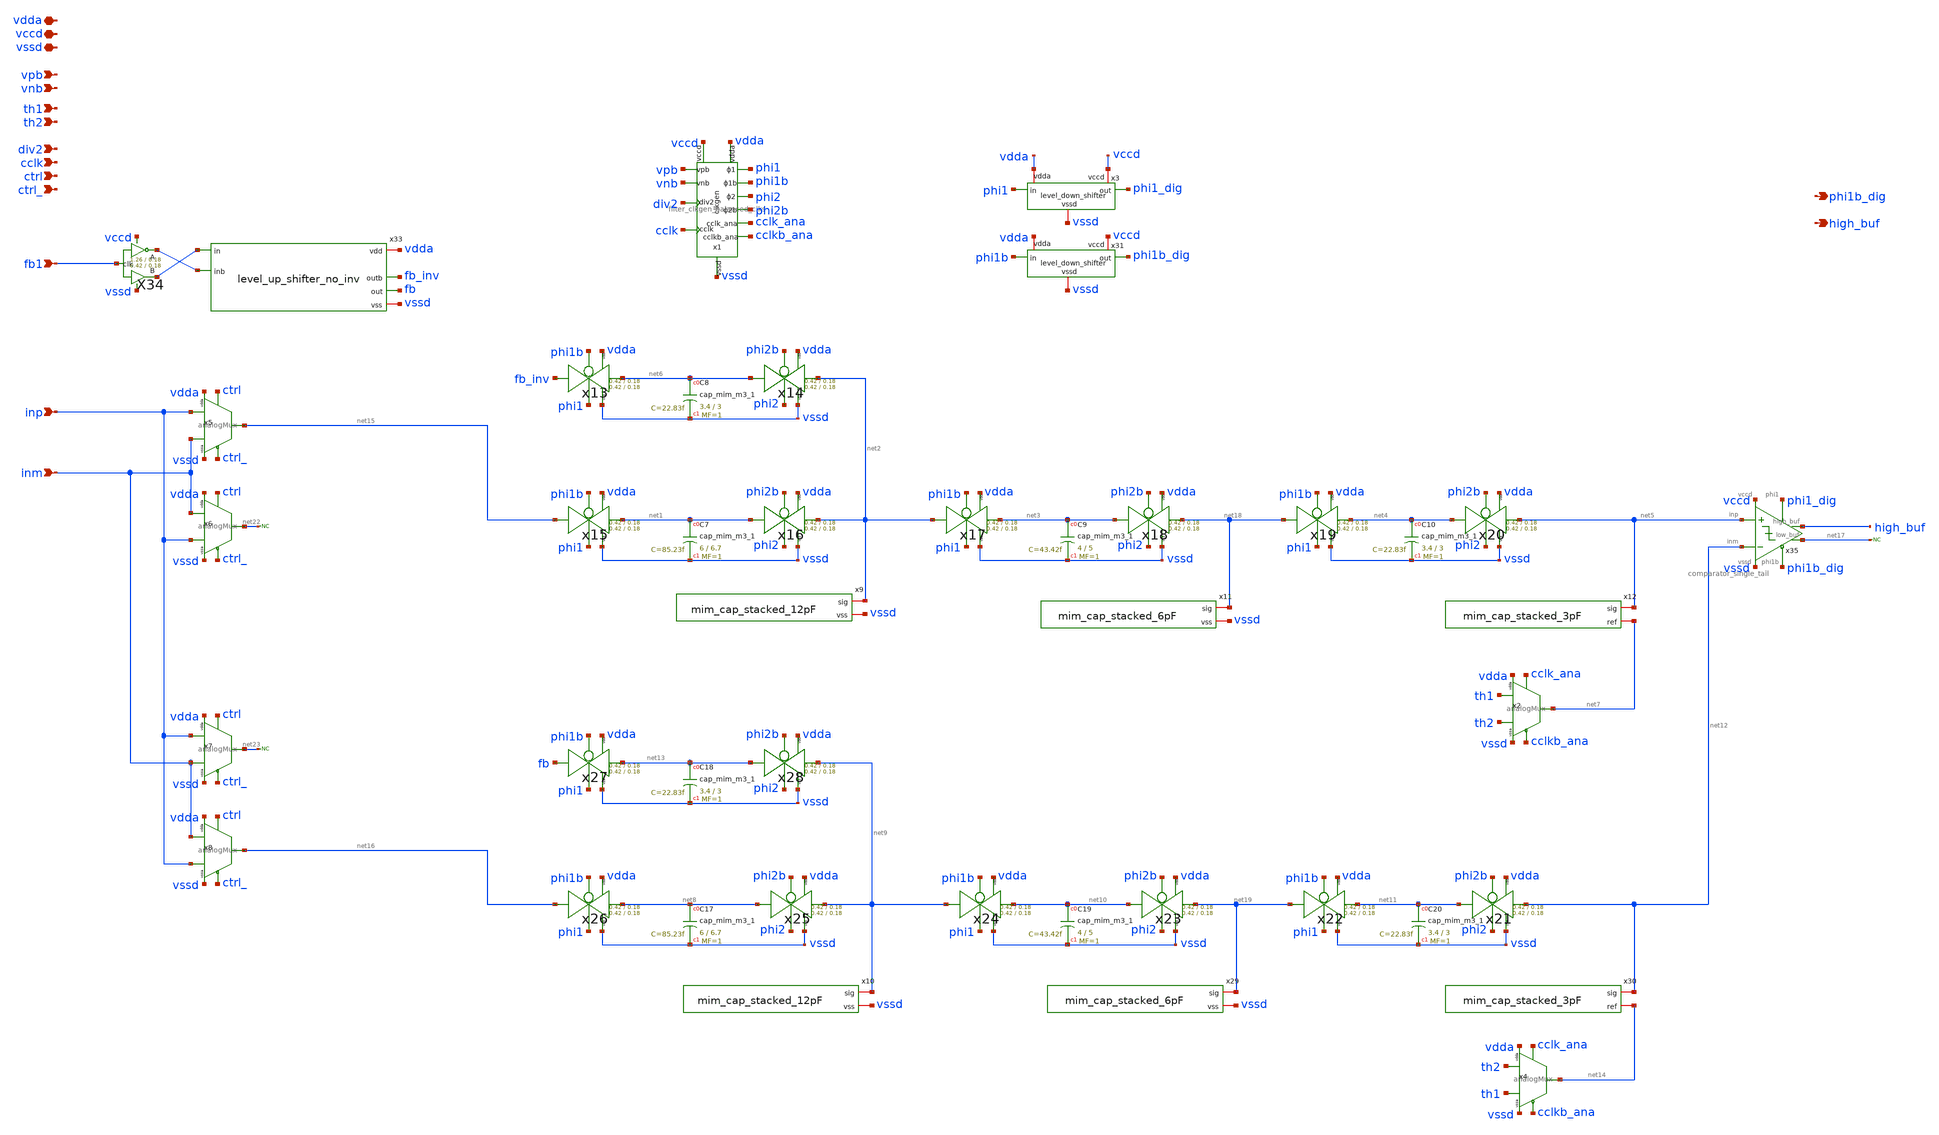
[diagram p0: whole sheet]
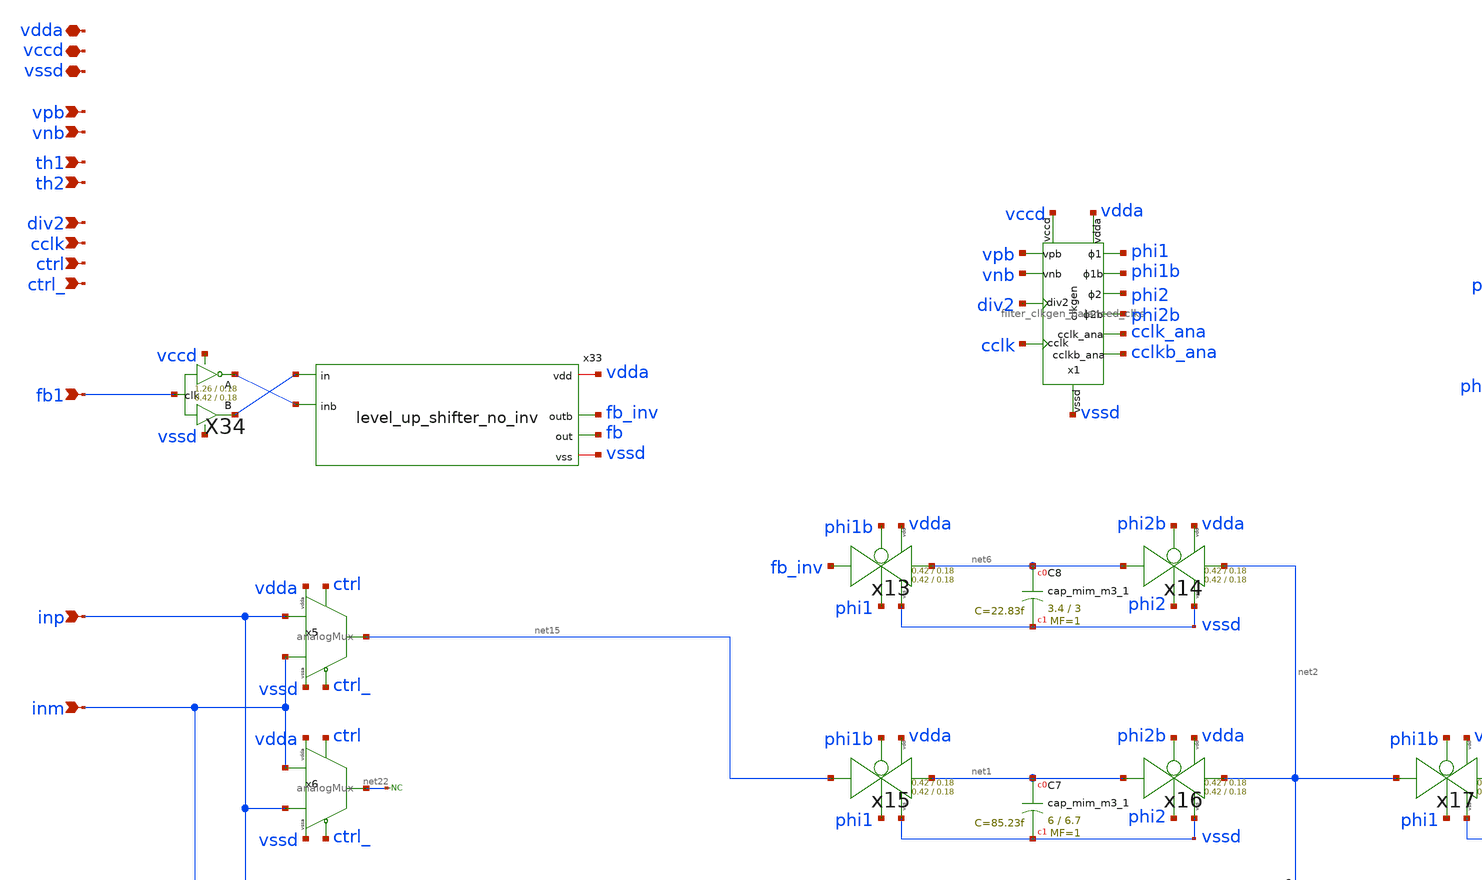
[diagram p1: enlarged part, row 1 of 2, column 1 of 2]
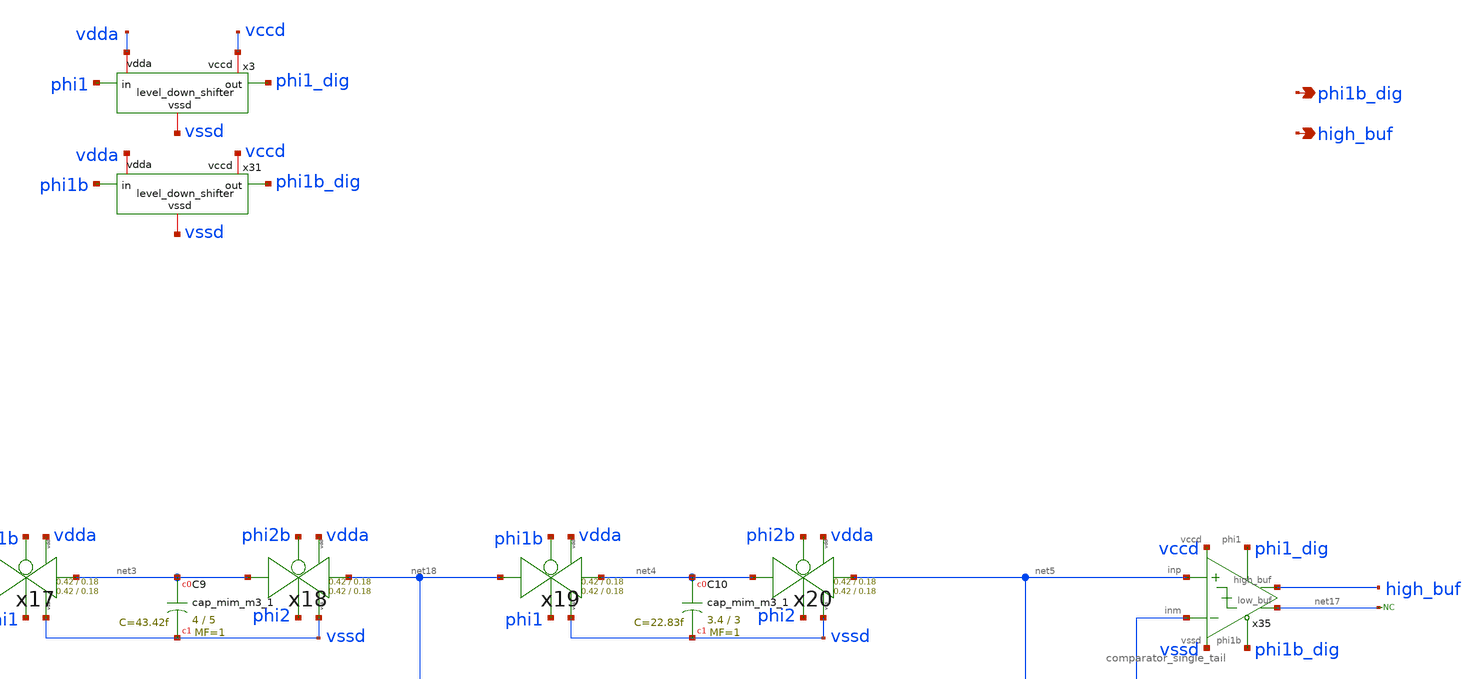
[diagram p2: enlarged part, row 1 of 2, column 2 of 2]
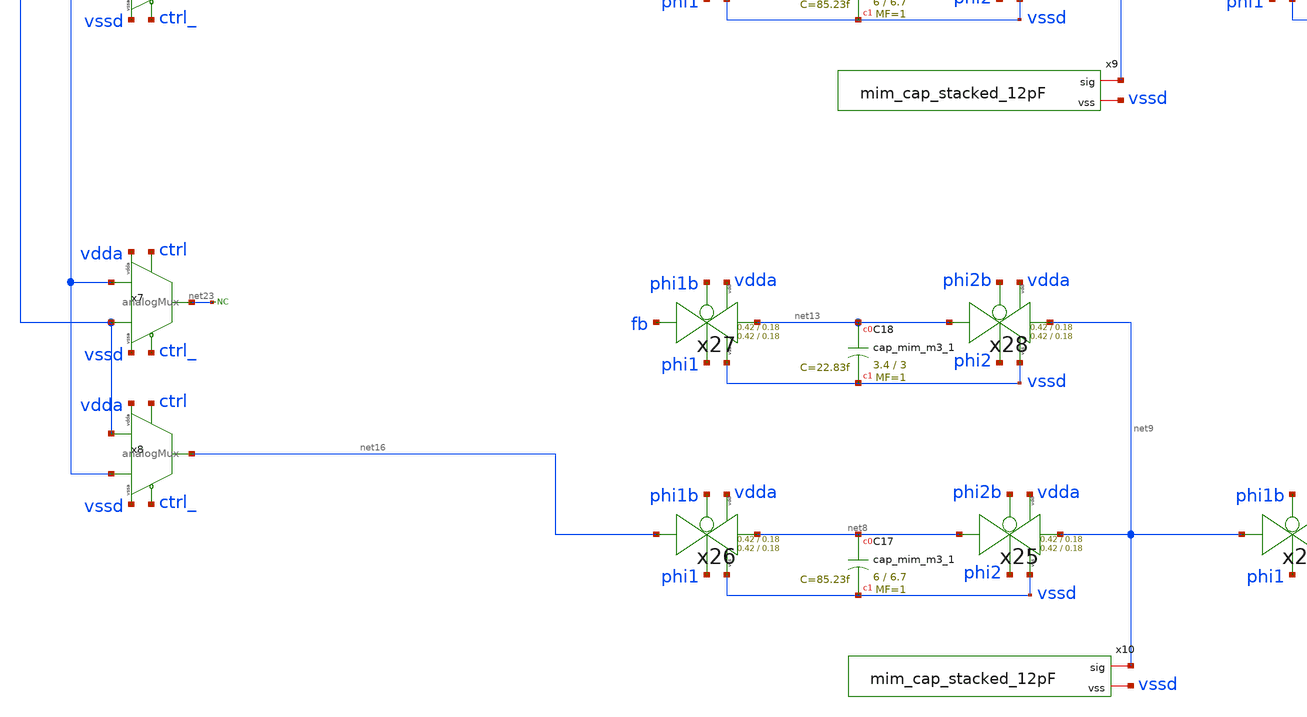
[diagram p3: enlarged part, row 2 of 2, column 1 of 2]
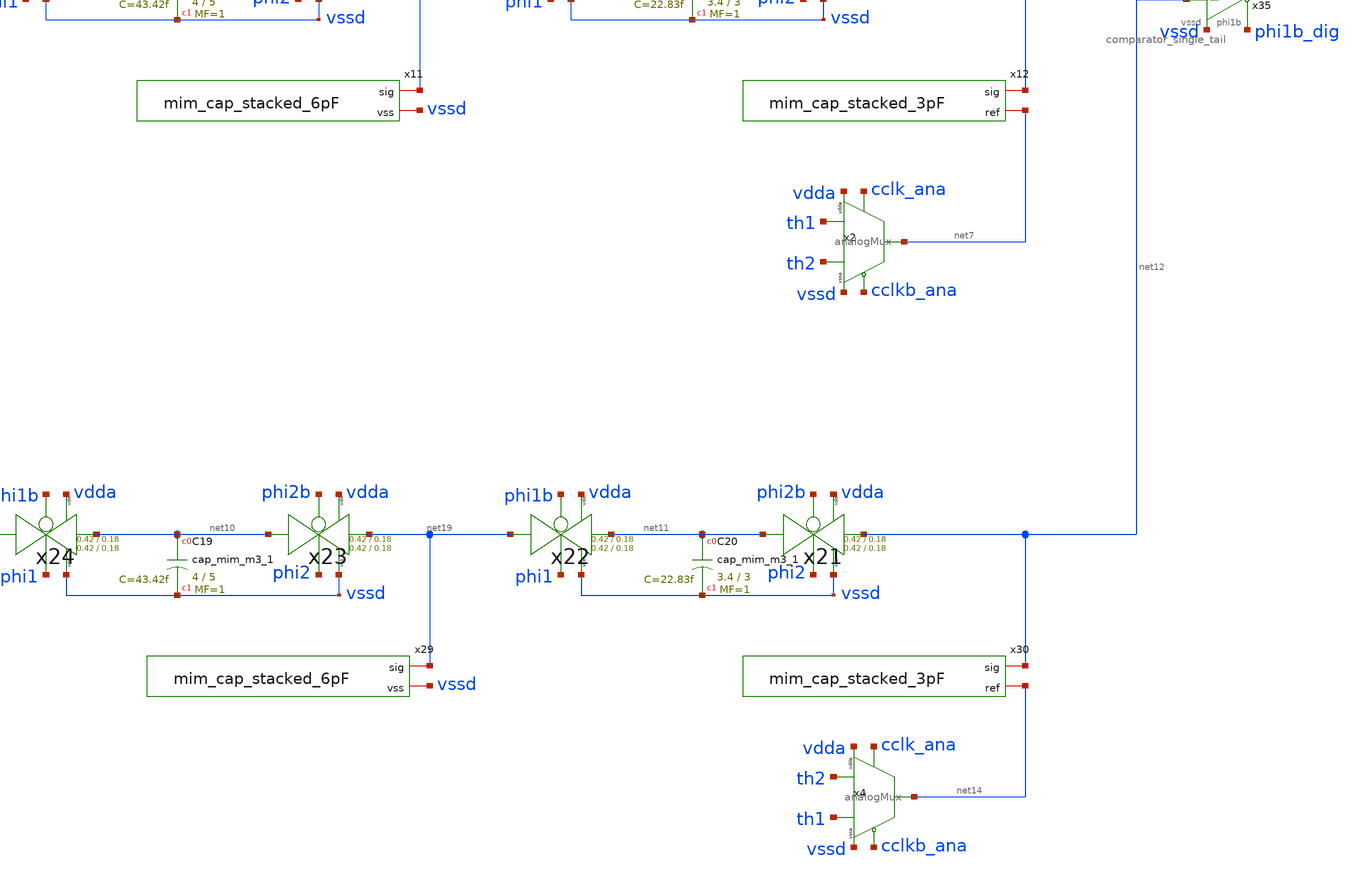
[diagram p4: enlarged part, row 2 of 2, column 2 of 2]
** sch_path: xschem/tryandtest/for_lvs.sch
**.subckt for_lvs inp inm vdda ctrl ctrl_ vccd fb1 vssd vpb vnb div2 cclk phi1b_dig high_buf th1 th2
*.ipin inp
*.ipin inm
*.iopin vdda
*.ipin ctrl
*.ipin ctrl_
*.iopin vccd
*.ipin fb1
*.iopin vssd
*.ipin vpb
*.ipin vnb
*.ipin div2
*.ipin cclk
*.opin phi1b_dig
*.opin high_buf
*.ipin th1
*.ipin th2
x1 cclk phi2b phi2 phi1b phi1 cclkb_ana cclk_ana vpb vnb vdda vssd vccd div2
+ filter_clkgen_balanced_clks
XC7 net1 vssd sky130_fd_pr__cap_mim_m3_1 W=6 L=6.7 MF=1 m=1
XC8 net6 vssd sky130_fd_pr__cap_mim_m3_1 W=3.4 L=3 MF=1 m=1
XC9 net3 vssd sky130_fd_pr__cap_mim_m3_1 W=4 L=5 MF=1 m=1
XC10 net4 vssd sky130_fd_pr__cap_mim_m3_1 W=3.4 L=3 MF=1 m=1
x2 th2 th1 cclk_ana cclkb_ana net7 vssd vdda analogMux
XC17 net8 vssd sky130_fd_pr__cap_mim_m3_1 W=6 L=6.7 MF=1 m=1
XC18 net13 vssd sky130_fd_pr__cap_mim_m3_1 W=3.4 L=3 MF=1 m=1
XC19 net10 vssd sky130_fd_pr__cap_mim_m3_1 W=4 L=5 MF=1 m=1
XC20 net11 vssd sky130_fd_pr__cap_mim_m3_1 W=3.4 L=3 MF=1 m=1
x4 th1 th2 cclk_ana cclkb_ana net14 vssd vdda analogMux
x5 inm inp ctrl ctrl_ net15 vssd vdda analogMux
x6 inp inm ctrl ctrl_ net22 vssd vdda analogMux
x7 inm inp ctrl ctrl_ net23 vssd vdda analogMux
x8 inp inm ctrl ctrl_ net16 vssd vdda analogMux
x13 fb_inv net6 phi1b phi1 vdda vssd tg Wpmos=0.42 Lpmos=0.18 Wnmos=0.42 Lnmos=0.18
x14 net6 net2 phi2b phi2 vdda vssd tg Wpmos=0.42 Lpmos=0.18 Wnmos=0.42 Lnmos=0.18
x15 net15 net1 phi1b phi1 vdda vssd tg Wpmos=0.42 Lpmos=0.18 Wnmos=0.42 Lnmos=0.18
x16 net1 net2 phi2b phi2 vdda vssd tg Wpmos=0.42 Lpmos=0.18 Wnmos=0.42 Lnmos=0.18
x17 net2 net3 phi1b phi1 vdda vssd tg Wpmos=0.42 Lpmos=0.18 Wnmos=0.42 Lnmos=0.18
x18 net3 net18 phi2b phi2 vdda vssd tg Wpmos=0.42 Lpmos=0.18 Wnmos=0.42 Lnmos=0.18
x19 net18 net4 phi1b phi1 vdda vssd tg Wpmos=0.42 Lpmos=0.18 Wnmos=0.42 Lnmos=0.18
x20 net4 net5 phi2b phi2 vdda vssd tg Wpmos=0.42 Lpmos=0.18 Wnmos=0.42 Lnmos=0.18
x21 net11 net12 phi2b phi2 vdda vssd tg Wpmos=0.42 Lpmos=0.18 Wnmos=0.42 Lnmos=0.18
x22 net19 net11 phi1b phi1 vdda vssd tg Wpmos=0.42 Lpmos=0.18 Wnmos=0.42 Lnmos=0.18
x23 net10 net19 phi2b phi2 vdda vssd tg Wpmos=0.42 Lpmos=0.18 Wnmos=0.42 Lnmos=0.18
x24 net9 net10 phi1b phi1 vdda vssd tg Wpmos=0.42 Lpmos=0.18 Wnmos=0.42 Lnmos=0.18
x25 net8 net9 phi2b phi2 vdda vssd tg Wpmos=0.42 Lpmos=0.18 Wnmos=0.42 Lnmos=0.18
x26 net16 net8 phi1b phi1 vdda vssd tg Wpmos=0.42 Lpmos=0.18 Wnmos=0.42 Lnmos=0.18
x27 fb net13 phi1b phi1 vdda vssd tg Wpmos=0.42 Lpmos=0.18 Wnmos=0.42 Lnmos=0.18
x28 net13 net9 phi2b phi2 vdda vssd tg Wpmos=0.42 Lpmos=0.18 Wnmos=0.42 Lnmos=0.18
x9 net2 vssd mim_cap_stacked_12pF
x10 net9 vssd mim_cap_stacked_12pF
x11 net18 vssd mim_cap_stacked_6pF
x12 net5 net7 mim_cap_stacked_3pF
x29 net19 vssd mim_cap_stacked_6pF
x30 net12 net14 mim_cap_stacked_3pF
x33 vdda net21 fb_inv fb vssd net20 level_up_shifter_no_inv
X34 fb1 net20 net21 vccd vssd comp_clks_1stage Wpmos=1.26 Lpmos=0.18 Wnmos=0.42 Lnmos=0.18
x35 net5 net12 high_buf phi1_dig phi1b_dig net17 vccd vssd comparator_single_tail Wplus=0.42
+ Lplus=0.42 Wminus=0.42 Lminus=0.15
* noconn #net22
* noconn #net23
* noconn #net17
x3 vdda vccd phi1 phi1_dig vssd level_down_shifter
x31 vdda vccd phi1b phi1b_dig vssd level_down_shifter
**** begin user architecture code
 .lib $::SKYWATER_MODELS/sky130.lib.spice tt
.include $::SKYWATER_STDCELLS/sky130_fd_sc_hd.spice

**** end user architecture code
**.ends
.end
